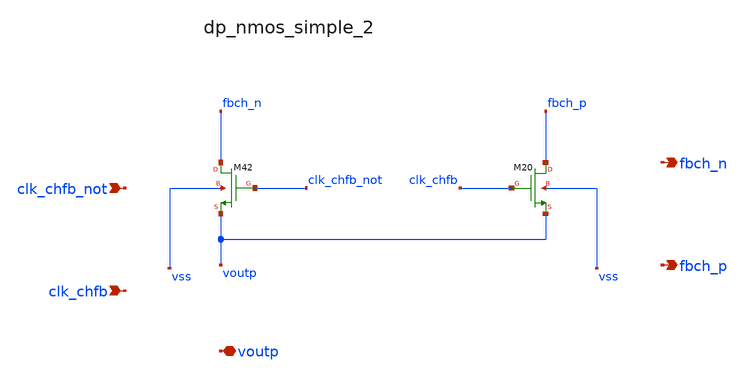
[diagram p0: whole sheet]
** sch_path: analog-db/raw/ia_003_fan_chopper_pf/hier/blocks/dp_nmos_simple_2.sch
**.subckt dp_nmos_simple_2 clk_chfb_not clk_chfb voutp fbch_n fbch_p
*.ipin clk_chfb_not
*.ipin clk_chfb
*.iopin voutp
*.opin fbch_n
*.opin fbch_p
XM20 fbch_p clk_chfb voutp vss sg13_lv_nmos w=x_dut_xm20_w l=x_dut_xm20_l ng=1 m=x_dut_xm20_m
XM42 fbch_n clk_chfb_not voutp vss sg13_lv_nmos w=x_dut_xm42_w l=x_dut_xm42_l ng=1 m=x_dut_xm42_m
**.ends
.end
